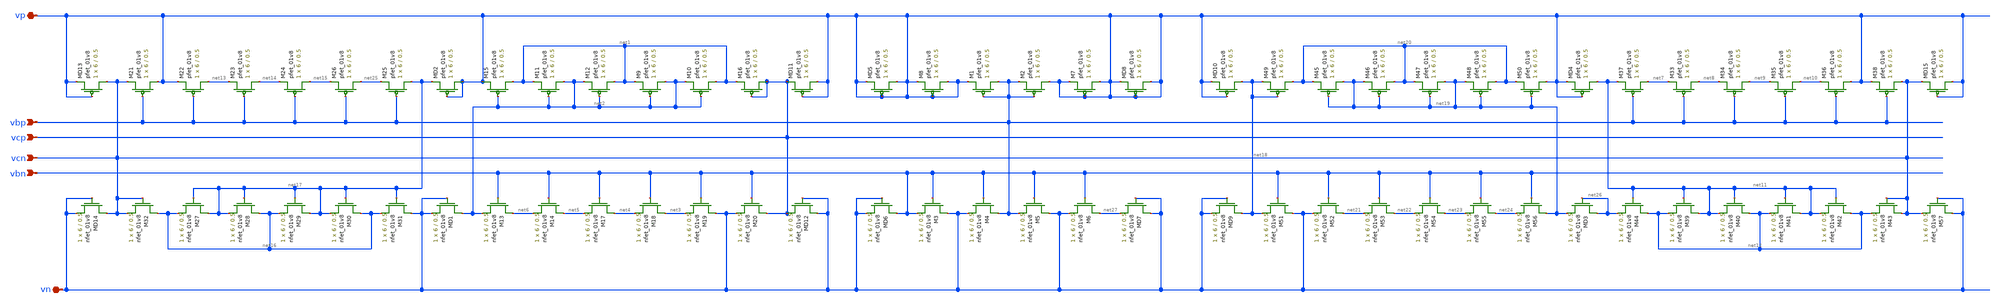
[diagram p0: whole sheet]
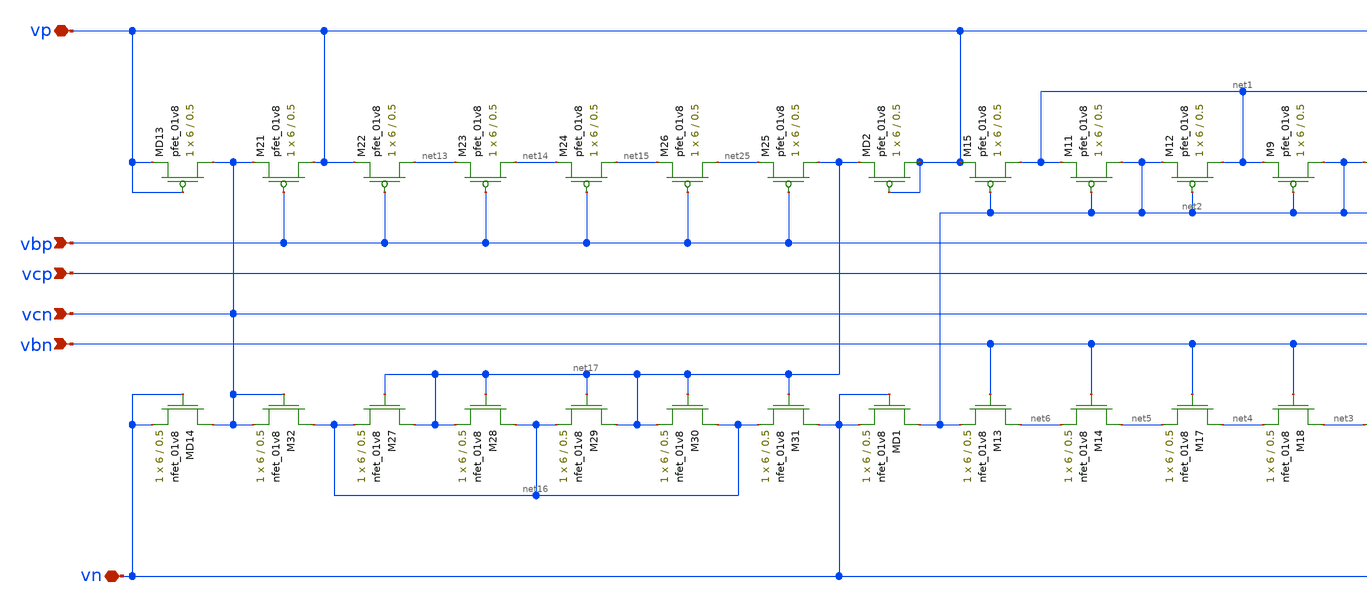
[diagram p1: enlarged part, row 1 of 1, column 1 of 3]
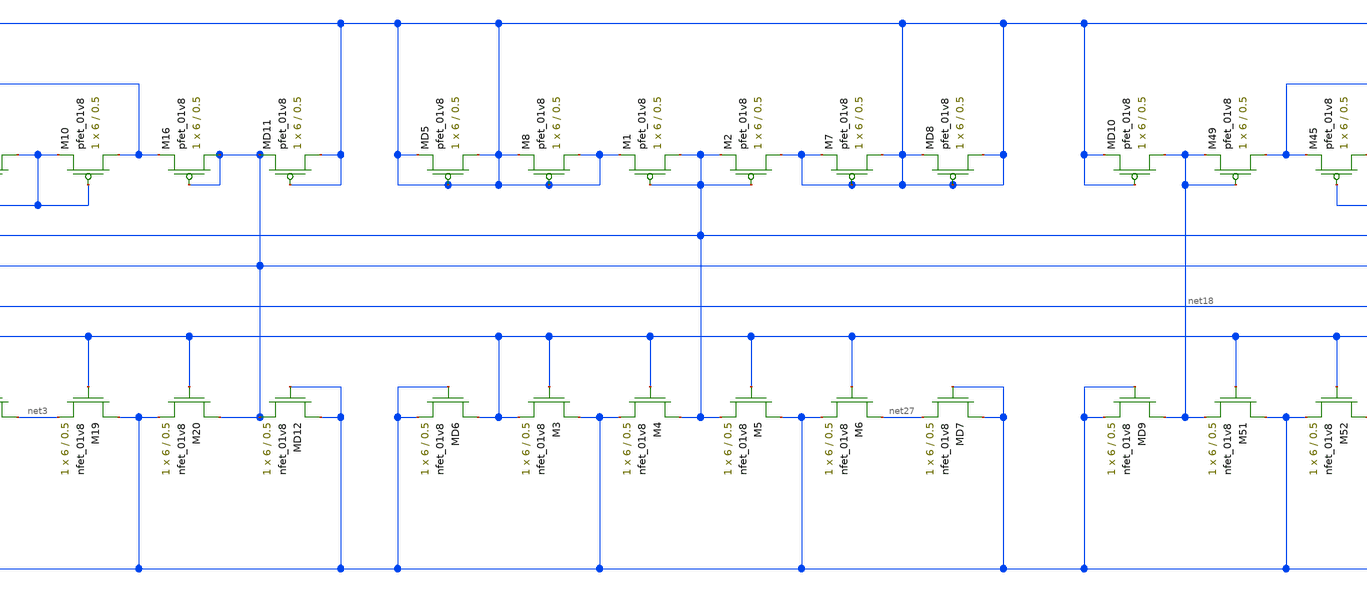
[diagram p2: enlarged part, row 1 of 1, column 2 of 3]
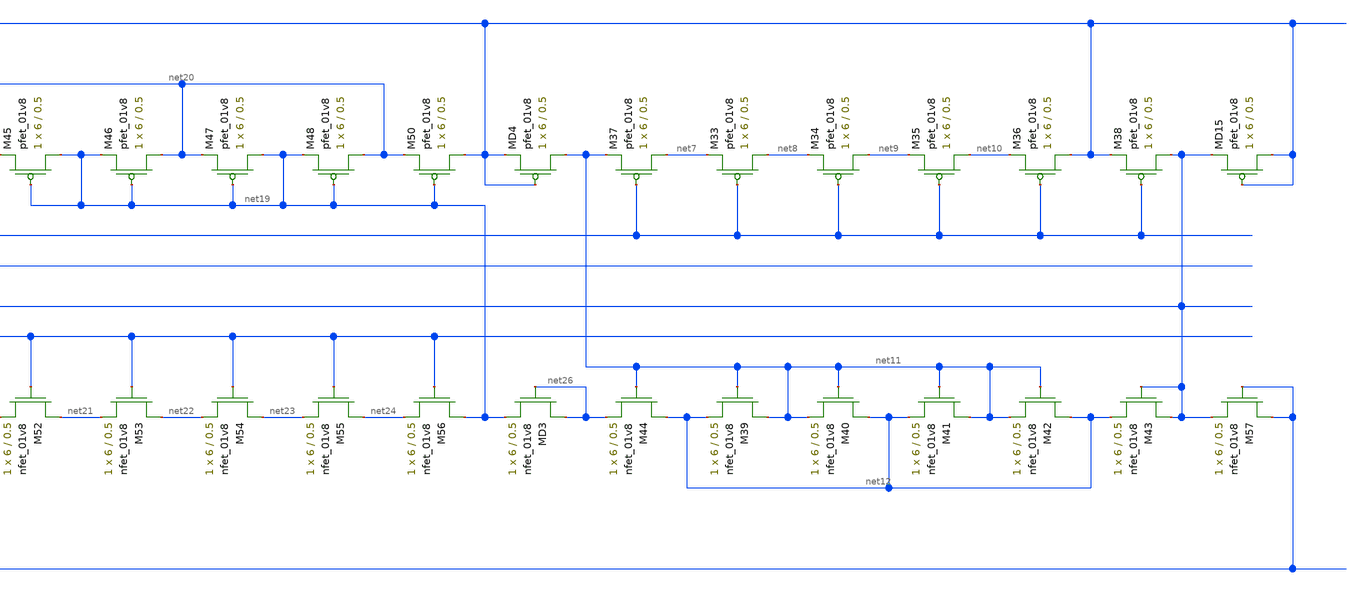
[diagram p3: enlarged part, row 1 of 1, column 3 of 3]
** sch_path: mini_proj_3/schematic/bias_generator.sch
**.subckt bias_generator vp vn vbn vcn vcp vbp
*.iopin vp
*.iopin vn
*.ipin vbn
*.ipin vcn
*.ipin vcp
*.ipin vbp
XM3 vn vbn vbn GND sky130_fd_pr__nfet_01v8 L=0.5 W=6 nf=1 ad='int((nf+1)/2) * W/nf * 0.29' as='int((nf+2)/2) * W/nf * 0.29'
+ pd='2*int((nf+1)/2) * (W/nf + 0.29)' ps='2*int((nf+2)/2) * (W/nf + 0.29)' nrd='0.29 / W' nrs='0.29 / W'
+ sa=0 sb=0 sd=0 mult=1 m=1
XM8 vp vp vp VDD sky130_fd_pr__pfet_01v8 L=0.5 W=6 nf=1 ad='int((nf+1)/2) * W/nf * 0.29' as='int((nf+2)/2) * W/nf * 0.29'
+ pd='2*int((nf+1)/2) * (W/nf + 0.29)' ps='2*int((nf+2)/2) * (W/nf + 0.29)' nrd='0.29 / W' nrs='0.29 / W'
+ sa=0 sb=0 sd=0 mult=1 m=1
XM1 vbp vbp vp VDD sky130_fd_pr__pfet_01v8 L=0.5 W=6 nf=1 ad='int((nf+1)/2) * W/nf * 0.29' as='int((nf+2)/2) * W/nf * 0.29'
+ pd='2*int((nf+1)/2) * (W/nf + 0.29)' ps='2*int((nf+2)/2) * (W/nf + 0.29)' nrd='0.29 / W' nrs='0.29 / W'
+ sa=0 sb=0 sd=0 mult=1 m=1
XM2 vp vbp vbp VDD sky130_fd_pr__pfet_01v8 L=0.5 W=6 nf=1 ad='int((nf+1)/2) * W/nf * 0.29' as='int((nf+2)/2) * W/nf * 0.29'
+ pd='2*int((nf+1)/2) * (W/nf + 0.29)' ps='2*int((nf+2)/2) * (W/nf + 0.29)' nrd='0.29 / W' nrs='0.29 / W'
+ sa=0 sb=0 sd=0 mult=1 m=1
XM7 vp vp vp VDD sky130_fd_pr__pfet_01v8 L=0.5 W=6 nf=1 ad='int((nf+1)/2) * W/nf * 0.29' as='int((nf+2)/2) * W/nf * 0.29'
+ pd='2*int((nf+1)/2) * (W/nf + 0.29)' ps='2*int((nf+2)/2) * (W/nf + 0.29)' nrd='0.29 / W' nrs='0.29 / W'
+ sa=0 sb=0 sd=0 mult=1 m=1
XM4 vbp vbn vn GND sky130_fd_pr__nfet_01v8 L=0.5 W=6 nf=1 ad='int((nf+1)/2) * W/nf * 0.29' as='int((nf+2)/2) * W/nf * 0.29'
+ pd='2*int((nf+1)/2) * (W/nf + 0.29)' ps='2*int((nf+2)/2) * (W/nf + 0.29)' nrd='0.29 / W' nrs='0.29 / W'
+ sa=0 sb=0 sd=0 mult=1 m=1
XM5 vn vbn vbp GND sky130_fd_pr__nfet_01v8 L=0.5 W=6 nf=1 ad='int((nf+1)/2) * W/nf * 0.29' as='int((nf+2)/2) * W/nf * 0.29'
+ pd='2*int((nf+1)/2) * (W/nf + 0.29)' ps='2*int((nf+2)/2) * (W/nf + 0.29)' nrd='0.29 / W' nrs='0.29 / W'
+ sa=0 sb=0 sd=0 mult=1 m=1
XM6 net27 vbn vn GND sky130_fd_pr__nfet_01v8 L=0.5 W=6 nf=1 ad='int((nf+1)/2) * W/nf * 0.29' as='int((nf+2)/2) * W/nf * 0.29'
+ pd='2*int((nf+1)/2) * (W/nf + 0.29)' ps='2*int((nf+2)/2) * (W/nf + 0.29)' nrd='0.29 / W' nrs='0.29 / W'
+ sa=0 sb=0 sd=0 mult=1 m=1
XM11 net2 net2 net1 VDD sky130_fd_pr__pfet_01v8 L=0.5 W=6 nf=1 ad='int((nf+1)/2) * W/nf * 0.29' as='int((nf+2)/2) * W/nf * 0.29'
+ pd='2*int((nf+1)/2) * (W/nf + 0.29)' ps='2*int((nf+2)/2) * (W/nf + 0.29)' nrd='0.29 / W' nrs='0.29 / W'
+ sa=0 sb=0 sd=0 mult=1 m=1
XM12 net1 net2 net2 VDD sky130_fd_pr__pfet_01v8 L=0.5 W=6 nf=1 ad='int((nf+1)/2) * W/nf * 0.29' as='int((nf+2)/2) * W/nf * 0.29'
+ pd='2*int((nf+1)/2) * (W/nf + 0.29)' ps='2*int((nf+2)/2) * (W/nf + 0.29)' nrd='0.29 / W' nrs='0.29 / W'
+ sa=0 sb=0 sd=0 mult=1 m=1
XM9 net2 net2 net1 VDD sky130_fd_pr__pfet_01v8 L=0.5 W=6 nf=1 ad='int((nf+1)/2) * W/nf * 0.29' as='int((nf+2)/2) * W/nf * 0.29'
+ pd='2*int((nf+1)/2) * (W/nf + 0.29)' ps='2*int((nf+2)/2) * (W/nf + 0.29)' nrd='0.29 / W' nrs='0.29 / W'
+ sa=0 sb=0 sd=0 mult=1 m=1
XM10 net1 net2 net2 VDD sky130_fd_pr__pfet_01v8 L=0.5 W=6 nf=1 ad='int((nf+1)/2) * W/nf * 0.29' as='int((nf+2)/2) * W/nf * 0.29'
+ pd='2*int((nf+1)/2) * (W/nf + 0.29)' ps='2*int((nf+2)/2) * (W/nf + 0.29)' nrd='0.29 / W' nrs='0.29 / W'
+ sa=0 sb=0 sd=0 mult=1 m=1
XM15 net1 net2 vp VDD sky130_fd_pr__pfet_01v8 L=0.5 W=6 nf=1 ad='int((nf+1)/2) * W/nf * 0.29' as='int((nf+2)/2) * W/nf * 0.29'
+ pd='2*int((nf+1)/2) * (W/nf + 0.29)' ps='2*int((nf+2)/2) * (W/nf + 0.29)' nrd='0.29 / W' nrs='0.29 / W'
+ sa=0 sb=0 sd=0 mult=1 m=1
XM16 vcp vcp net1 VDD sky130_fd_pr__pfet_01v8 L=0.5 W=6 nf=1 ad='int((nf+1)/2) * W/nf * 0.29' as='int((nf+2)/2) * W/nf * 0.29'
+ pd='2*int((nf+1)/2) * (W/nf + 0.29)' ps='2*int((nf+2)/2) * (W/nf + 0.29)' nrd='0.29 / W' nrs='0.29 / W'
+ sa=0 sb=0 sd=0 mult=1 m=1
XM13 net6 vbn net2 GND sky130_fd_pr__nfet_01v8 L=0.5 W=6 nf=1 ad='int((nf+1)/2) * W/nf * 0.29' as='int((nf+2)/2) * W/nf * 0.29'
+ pd='2*int((nf+1)/2) * (W/nf + 0.29)' ps='2*int((nf+2)/2) * (W/nf + 0.29)' nrd='0.29 / W' nrs='0.29 / W'
+ sa=0 sb=0 sd=0 mult=1 m=1
XM14 net5 vbn net6 GND sky130_fd_pr__nfet_01v8 L=0.5 W=6 nf=1 ad='int((nf+1)/2) * W/nf * 0.29' as='int((nf+2)/2) * W/nf * 0.29'
+ pd='2*int((nf+1)/2) * (W/nf + 0.29)' ps='2*int((nf+2)/2) * (W/nf + 0.29)' nrd='0.29 / W' nrs='0.29 / W'
+ sa=0 sb=0 sd=0 mult=1 m=1
XM17 net4 vbn net5 GND sky130_fd_pr__nfet_01v8 L=0.5 W=6 nf=1 ad='int((nf+1)/2) * W/nf * 0.29' as='int((nf+2)/2) * W/nf * 0.29'
+ pd='2*int((nf+1)/2) * (W/nf + 0.29)' ps='2*int((nf+2)/2) * (W/nf + 0.29)' nrd='0.29 / W' nrs='0.29 / W'
+ sa=0 sb=0 sd=0 mult=1 m=1
XM18 net3 vbn net4 GND sky130_fd_pr__nfet_01v8 L=0.5 W=6 nf=1 ad='int((nf+1)/2) * W/nf * 0.29' as='int((nf+2)/2) * W/nf * 0.29'
+ pd='2*int((nf+1)/2) * (W/nf + 0.29)' ps='2*int((nf+2)/2) * (W/nf + 0.29)' nrd='0.29 / W' nrs='0.29 / W'
+ sa=0 sb=0 sd=0 mult=1 m=1
XM19 vn vbn net3 GND sky130_fd_pr__nfet_01v8 L=0.5 W=6 nf=1 ad='int((nf+1)/2) * W/nf * 0.29' as='int((nf+2)/2) * W/nf * 0.29'
+ pd='2*int((nf+1)/2) * (W/nf + 0.29)' ps='2*int((nf+2)/2) * (W/nf + 0.29)' nrd='0.29 / W' nrs='0.29 / W'
+ sa=0 sb=0 sd=0 mult=1 m=1
XM20 vcp vbn vn GND sky130_fd_pr__nfet_01v8 L=0.5 W=6 nf=1 ad='int((nf+1)/2) * W/nf * 0.29' as='int((nf+2)/2) * W/nf * 0.29'
+ pd='2*int((nf+1)/2) * (W/nf + 0.29)' ps='2*int((nf+2)/2) * (W/nf + 0.29)' nrd='0.29 / W' nrs='0.29 / W'
+ sa=0 sb=0 sd=0 mult=1 m=1
XM33 net8 vbp net7 VDD sky130_fd_pr__pfet_01v8 L=0.5 W=6 nf=1 ad='int((nf+1)/2) * W/nf * 0.29' as='int((nf+2)/2) * W/nf * 0.29'
+ pd='2*int((nf+1)/2) * (W/nf + 0.29)' ps='2*int((nf+2)/2) * (W/nf + 0.29)' nrd='0.29 / W' nrs='0.29 / W'
+ sa=0 sb=0 sd=0 mult=1 m=1
XM34 net9 vbp net8 VDD sky130_fd_pr__pfet_01v8 L=0.5 W=6 nf=1 ad='int((nf+1)/2) * W/nf * 0.29' as='int((nf+2)/2) * W/nf * 0.29'
+ pd='2*int((nf+1)/2) * (W/nf + 0.29)' ps='2*int((nf+2)/2) * (W/nf + 0.29)' nrd='0.29 / W' nrs='0.29 / W'
+ sa=0 sb=0 sd=0 mult=1 m=1
XM35 net10 vbp net9 VDD sky130_fd_pr__pfet_01v8 L=0.5 W=6 nf=1 ad='int((nf+1)/2) * W/nf * 0.29' as='int((nf+2)/2) * W/nf * 0.29'
+ pd='2*int((nf+1)/2) * (W/nf + 0.29)' ps='2*int((nf+2)/2) * (W/nf + 0.29)' nrd='0.29 / W' nrs='0.29 / W'
+ sa=0 sb=0 sd=0 mult=1 m=1
XM36 vp vbp net10 VDD sky130_fd_pr__pfet_01v8 L=0.5 W=6 nf=1 ad='int((nf+1)/2) * W/nf * 0.29' as='int((nf+2)/2) * W/nf * 0.29'
+ pd='2*int((nf+1)/2) * (W/nf + 0.29)' ps='2*int((nf+2)/2) * (W/nf + 0.29)' nrd='0.29 / W' nrs='0.29 / W'
+ sa=0 sb=0 sd=0 mult=1 m=1
XM37 net7 vbp net11 VDD sky130_fd_pr__pfet_01v8 L=0.5 W=6 nf=1 ad='int((nf+1)/2) * W/nf * 0.29' as='int((nf+2)/2) * W/nf * 0.29'
+ pd='2*int((nf+1)/2) * (W/nf + 0.29)' ps='2*int((nf+2)/2) * (W/nf + 0.29)' nrd='0.29 / W' nrs='0.29 / W'
+ sa=0 sb=0 sd=0 mult=1 m=1
XM38 vcn vbp vp VDD sky130_fd_pr__pfet_01v8 L=0.5 W=6 nf=1 ad='int((nf+1)/2) * W/nf * 0.29' as='int((nf+2)/2) * W/nf * 0.29'
+ pd='2*int((nf+1)/2) * (W/nf + 0.29)' ps='2*int((nf+2)/2) * (W/nf + 0.29)' nrd='0.29 / W' nrs='0.29 / W'
+ sa=0 sb=0 sd=0 mult=1 m=1
XM39 net11 net11 net12 GND sky130_fd_pr__nfet_01v8 L=0.5 W=6 nf=1 ad='int((nf+1)/2) * W/nf * 0.29' as='int((nf+2)/2) * W/nf * 0.29'
+ pd='2*int((nf+1)/2) * (W/nf + 0.29)' ps='2*int((nf+2)/2) * (W/nf + 0.29)' nrd='0.29 / W' nrs='0.29 / W'
+ sa=0 sb=0 sd=0 mult=1 m=1
XM40 net12 net11 net11 GND sky130_fd_pr__nfet_01v8 L=0.5 W=6 nf=1 ad='int((nf+1)/2) * W/nf * 0.29' as='int((nf+2)/2) * W/nf * 0.29'
+ pd='2*int((nf+1)/2) * (W/nf + 0.29)' ps='2*int((nf+2)/2) * (W/nf + 0.29)' nrd='0.29 / W' nrs='0.29 / W'
+ sa=0 sb=0 sd=0 mult=1 m=1
XM41 net11 net11 net12 GND sky130_fd_pr__nfet_01v8 L=0.5 W=6 nf=1 ad='int((nf+1)/2) * W/nf * 0.29' as='int((nf+2)/2) * W/nf * 0.29'
+ pd='2*int((nf+1)/2) * (W/nf + 0.29)' ps='2*int((nf+2)/2) * (W/nf + 0.29)' nrd='0.29 / W' nrs='0.29 / W'
+ sa=0 sb=0 sd=0 mult=1 m=1
XM42 net12 net11 net11 GND sky130_fd_pr__nfet_01v8 L=0.5 W=6 nf=1 ad='int((nf+1)/2) * W/nf * 0.29' as='int((nf+2)/2) * W/nf * 0.29'
+ pd='2*int((nf+1)/2) * (W/nf + 0.29)' ps='2*int((nf+2)/2) * (W/nf + 0.29)' nrd='0.29 / W' nrs='0.29 / W'
+ sa=0 sb=0 sd=0 mult=1 m=1
XM43 vcn vcn net12 GND sky130_fd_pr__nfet_01v8 L=0.5 W=6 nf=1 ad='int((nf+1)/2) * W/nf * 0.29' as='int((nf+2)/2) * W/nf * 0.29'
+ pd='2*int((nf+1)/2) * (W/nf + 0.29)' ps='2*int((nf+2)/2) * (W/nf + 0.29)' nrd='0.29 / W' nrs='0.29 / W'
+ sa=0 sb=0 sd=0 mult=1 m=1
XM44 net12 net11 net26 GND sky130_fd_pr__nfet_01v8 L=0.5 W=6 nf=1 ad='int((nf+1)/2) * W/nf * 0.29' as='int((nf+2)/2) * W/nf * 0.29'
+ pd='2*int((nf+1)/2) * (W/nf + 0.29)' ps='2*int((nf+2)/2) * (W/nf + 0.29)' nrd='0.29 / W' nrs='0.29 / W'
+ sa=0 sb=0 sd=0 mult=1 m=1
XM21 vp vbp vcn VDD sky130_fd_pr__pfet_01v8 L=0.5 W=6 nf=1 ad='int((nf+1)/2) * W/nf * 0.29' as='int((nf+2)/2) * W/nf * 0.29'
+ pd='2*int((nf+1)/2) * (W/nf + 0.29)' ps='2*int((nf+2)/2) * (W/nf + 0.29)' nrd='0.29 / W' nrs='0.29 / W'
+ sa=0 sb=0 sd=0 mult=1 m=1
XM22 net13 vbp vp VDD sky130_fd_pr__pfet_01v8 L=0.5 W=6 nf=1 ad='int((nf+1)/2) * W/nf * 0.29' as='int((nf+2)/2) * W/nf * 0.29'
+ pd='2*int((nf+1)/2) * (W/nf + 0.29)' ps='2*int((nf+2)/2) * (W/nf + 0.29)' nrd='0.29 / W' nrs='0.29 / W'
+ sa=0 sb=0 sd=0 mult=1 m=1
XM23 net14 vbp net13 VDD sky130_fd_pr__pfet_01v8 L=0.5 W=6 nf=1 ad='int((nf+1)/2) * W/nf * 0.29' as='int((nf+2)/2) * W/nf * 0.29'
+ pd='2*int((nf+1)/2) * (W/nf + 0.29)' ps='2*int((nf+2)/2) * (W/nf + 0.29)' nrd='0.29 / W' nrs='0.29 / W'
+ sa=0 sb=0 sd=0 mult=1 m=1
XM24 net15 vbp net14 VDD sky130_fd_pr__pfet_01v8 L=0.5 W=6 nf=1 ad='int((nf+1)/2) * W/nf * 0.29' as='int((nf+2)/2) * W/nf * 0.29'
+ pd='2*int((nf+1)/2) * (W/nf + 0.29)' ps='2*int((nf+2)/2) * (W/nf + 0.29)' nrd='0.29 / W' nrs='0.29 / W'
+ sa=0 sb=0 sd=0 mult=1 m=1
XM25 net17 vbp net25 VDD sky130_fd_pr__pfet_01v8 L=0.5 W=6 nf=1 ad='int((nf+1)/2) * W/nf * 0.29' as='int((nf+2)/2) * W/nf * 0.29'
+ pd='2*int((nf+1)/2) * (W/nf + 0.29)' ps='2*int((nf+2)/2) * (W/nf + 0.29)' nrd='0.29 / W' nrs='0.29 / W'
+ sa=0 sb=0 sd=0 mult=1 m=1
XM26 net25 vbp net15 VDD sky130_fd_pr__pfet_01v8 L=0.5 W=6 nf=1 ad='int((nf+1)/2) * W/nf * 0.29' as='int((nf+2)/2) * W/nf * 0.29'
+ pd='2*int((nf+1)/2) * (W/nf + 0.29)' ps='2*int((nf+2)/2) * (W/nf + 0.29)' nrd='0.29 / W' nrs='0.29 / W'
+ sa=0 sb=0 sd=0 mult=1 m=1
XM27 net17 net17 net16 GND sky130_fd_pr__nfet_01v8 L=0.5 W=6 nf=1 ad='int((nf+1)/2) * W/nf * 0.29' as='int((nf+2)/2) * W/nf * 0.29'
+ pd='2*int((nf+1)/2) * (W/nf + 0.29)' ps='2*int((nf+2)/2) * (W/nf + 0.29)' nrd='0.29 / W' nrs='0.29 / W'
+ sa=0 sb=0 sd=0 mult=1 m=1
XM28 net16 net17 net17 GND sky130_fd_pr__nfet_01v8 L=0.5 W=6 nf=1 ad='int((nf+1)/2) * W/nf * 0.29' as='int((nf+2)/2) * W/nf * 0.29'
+ pd='2*int((nf+1)/2) * (W/nf + 0.29)' ps='2*int((nf+2)/2) * (W/nf + 0.29)' nrd='0.29 / W' nrs='0.29 / W'
+ sa=0 sb=0 sd=0 mult=1 m=1
XM29 net17 net17 net16 GND sky130_fd_pr__nfet_01v8 L=0.5 W=6 nf=1 ad='int((nf+1)/2) * W/nf * 0.29' as='int((nf+2)/2) * W/nf * 0.29'
+ pd='2*int((nf+1)/2) * (W/nf + 0.29)' ps='2*int((nf+2)/2) * (W/nf + 0.29)' nrd='0.29 / W' nrs='0.29 / W'
+ sa=0 sb=0 sd=0 mult=1 m=1
XM30 net16 net17 net17 GND sky130_fd_pr__nfet_01v8 L=0.5 W=6 nf=1 ad='int((nf+1)/2) * W/nf * 0.29' as='int((nf+2)/2) * W/nf * 0.29'
+ pd='2*int((nf+1)/2) * (W/nf + 0.29)' ps='2*int((nf+2)/2) * (W/nf + 0.29)' nrd='0.29 / W' nrs='0.29 / W'
+ sa=0 sb=0 sd=0 mult=1 m=1
XM31 vn net17 net16 GND sky130_fd_pr__nfet_01v8 L=0.5 W=6 nf=1 ad='int((nf+1)/2) * W/nf * 0.29' as='int((nf+2)/2) * W/nf * 0.29'
+ pd='2*int((nf+1)/2) * (W/nf + 0.29)' ps='2*int((nf+2)/2) * (W/nf + 0.29)' nrd='0.29 / W' nrs='0.29 / W'
+ sa=0 sb=0 sd=0 mult=1 m=1
XM32 net16 vcn vcn GND sky130_fd_pr__nfet_01v8 L=0.5 W=6 nf=1 ad='int((nf+1)/2) * W/nf * 0.29' as='int((nf+2)/2) * W/nf * 0.29'
+ pd='2*int((nf+1)/2) * (W/nf + 0.29)' ps='2*int((nf+2)/2) * (W/nf + 0.29)' nrd='0.29 / W' nrs='0.29 / W'
+ sa=0 sb=0 sd=0 mult=1 m=1
XM45 net19 net19 net20 VDD sky130_fd_pr__pfet_01v8 L=0.5 W=6 nf=1 ad='int((nf+1)/2) * W/nf * 0.29' as='int((nf+2)/2) * W/nf * 0.29'
+ pd='2*int((nf+1)/2) * (W/nf + 0.29)' ps='2*int((nf+2)/2) * (W/nf + 0.29)' nrd='0.29 / W' nrs='0.29 / W'
+ sa=0 sb=0 sd=0 mult=1 m=1
XM46 net20 net19 net19 VDD sky130_fd_pr__pfet_01v8 L=0.5 W=6 nf=1 ad='int((nf+1)/2) * W/nf * 0.29' as='int((nf+2)/2) * W/nf * 0.29'
+ pd='2*int((nf+1)/2) * (W/nf + 0.29)' ps='2*int((nf+2)/2) * (W/nf + 0.29)' nrd='0.29 / W' nrs='0.29 / W'
+ sa=0 sb=0 sd=0 mult=1 m=1
XM47 net19 net19 net20 VDD sky130_fd_pr__pfet_01v8 L=0.5 W=6 nf=1 ad='int((nf+1)/2) * W/nf * 0.29' as='int((nf+2)/2) * W/nf * 0.29'
+ pd='2*int((nf+1)/2) * (W/nf + 0.29)' ps='2*int((nf+2)/2) * (W/nf + 0.29)' nrd='0.29 / W' nrs='0.29 / W'
+ sa=0 sb=0 sd=0 mult=1 m=1
XM48 net20 net19 net19 VDD sky130_fd_pr__pfet_01v8 L=0.5 W=6 nf=1 ad='int((nf+1)/2) * W/nf * 0.29' as='int((nf+2)/2) * W/nf * 0.29'
+ pd='2*int((nf+1)/2) * (W/nf + 0.29)' ps='2*int((nf+2)/2) * (W/nf + 0.29)' nrd='0.29 / W' nrs='0.29 / W'
+ sa=0 sb=0 sd=0 mult=1 m=1
XM49 net20 net18 net18 VDD sky130_fd_pr__pfet_01v8 L=0.5 W=6 nf=1 ad='int((nf+1)/2) * W/nf * 0.29' as='int((nf+2)/2) * W/nf * 0.29'
+ pd='2*int((nf+1)/2) * (W/nf + 0.29)' ps='2*int((nf+2)/2) * (W/nf + 0.29)' nrd='0.29 / W' nrs='0.29 / W'
+ sa=0 sb=0 sd=0 mult=1 m=1
XM50 vp net19 net20 VDD sky130_fd_pr__pfet_01v8 L=0.5 W=6 nf=1 ad='int((nf+1)/2) * W/nf * 0.29' as='int((nf+2)/2) * W/nf * 0.29'
+ pd='2*int((nf+1)/2) * (W/nf + 0.29)' ps='2*int((nf+2)/2) * (W/nf + 0.29)' nrd='0.29 / W' nrs='0.29 / W'
+ sa=0 sb=0 sd=0 mult=1 m=1
XM51 vn vbn net18 GND sky130_fd_pr__nfet_01v8 L=0.5 W=6 nf=1 ad='int((nf+1)/2) * W/nf * 0.29' as='int((nf+2)/2) * W/nf * 0.29'
+ pd='2*int((nf+1)/2) * (W/nf + 0.29)' ps='2*int((nf+2)/2) * (W/nf + 0.29)' nrd='0.29 / W' nrs='0.29 / W'
+ sa=0 sb=0 sd=0 mult=1 m=1
XM52 net21 vbn vn GND sky130_fd_pr__nfet_01v8 L=0.5 W=6 nf=1 ad='int((nf+1)/2) * W/nf * 0.29' as='int((nf+2)/2) * W/nf * 0.29'
+ pd='2*int((nf+1)/2) * (W/nf + 0.29)' ps='2*int((nf+2)/2) * (W/nf + 0.29)' nrd='0.29 / W' nrs='0.29 / W'
+ sa=0 sb=0 sd=0 mult=1 m=1
XM53 net22 vbn net21 GND sky130_fd_pr__nfet_01v8 L=0.5 W=6 nf=1 ad='int((nf+1)/2) * W/nf * 0.29' as='int((nf+2)/2) * W/nf * 0.29'
+ pd='2*int((nf+1)/2) * (W/nf + 0.29)' ps='2*int((nf+2)/2) * (W/nf + 0.29)' nrd='0.29 / W' nrs='0.29 / W'
+ sa=0 sb=0 sd=0 mult=1 m=1
XM54 net23 vbn net22 GND sky130_fd_pr__nfet_01v8 L=0.5 W=6 nf=1 ad='int((nf+1)/2) * W/nf * 0.29' as='int((nf+2)/2) * W/nf * 0.29'
+ pd='2*int((nf+1)/2) * (W/nf + 0.29)' ps='2*int((nf+2)/2) * (W/nf + 0.29)' nrd='0.29 / W' nrs='0.29 / W'
+ sa=0 sb=0 sd=0 mult=1 m=1
XM55 net24 vbn net23 GND sky130_fd_pr__nfet_01v8 L=0.5 W=6 nf=1 ad='int((nf+1)/2) * W/nf * 0.29' as='int((nf+2)/2) * W/nf * 0.29'
+ pd='2*int((nf+1)/2) * (W/nf + 0.29)' ps='2*int((nf+2)/2) * (W/nf + 0.29)' nrd='0.29 / W' nrs='0.29 / W'
+ sa=0 sb=0 sd=0 mult=1 m=1
XM56 net19 vbn net24 GND sky130_fd_pr__nfet_01v8 L=0.5 W=6 nf=1 ad='int((nf+1)/2) * W/nf * 0.29' as='int((nf+2)/2) * W/nf * 0.29'
+ pd='2*int((nf+1)/2) * (W/nf + 0.29)' ps='2*int((nf+2)/2) * (W/nf + 0.29)' nrd='0.29 / W' nrs='0.29 / W'
+ sa=0 sb=0 sd=0 mult=1 m=1
XMD1 net2 vn vn GND sky130_fd_pr__nfet_01v8 L=0.5 W=6 nf=1 ad='int((nf+1)/2) * W/nf * 0.29' as='int((nf+2)/2) * W/nf * 0.29'
+ pd='2*int((nf+1)/2) * (W/nf + 0.29)' ps='2*int((nf+2)/2) * (W/nf + 0.29)' nrd='0.29 / W' nrs='0.29 / W'
+ sa=0 sb=0 sd=0 mult=1 m=1
XMD2 vp vp net17 VDD sky130_fd_pr__pfet_01v8 L=0.5 W=6 nf=1 ad='int((nf+1)/2) * W/nf * 0.29' as='int((nf+2)/2) * W/nf * 0.29'
+ pd='2*int((nf+1)/2) * (W/nf + 0.29)' ps='2*int((nf+2)/2) * (W/nf + 0.29)' nrd='0.29 / W' nrs='0.29 / W'
+ sa=0 sb=0 sd=0 mult=1 m=1
XMD3 net26 net26 net19 GND sky130_fd_pr__nfet_01v8 L=0.5 W=6 nf=1 ad='int((nf+1)/2) * W/nf * 0.29' as='int((nf+2)/2) * W/nf * 0.29'
+ pd='2*int((nf+1)/2) * (W/nf + 0.29)' ps='2*int((nf+2)/2) * (W/nf + 0.29)' nrd='0.29 / W' nrs='0.29 / W'
+ sa=0 sb=0 sd=0 mult=1 m=1
XMD4 net11 vp vp VDD sky130_fd_pr__pfet_01v8 L=0.5 W=6 nf=1 ad='int((nf+1)/2) * W/nf * 0.29' as='int((nf+2)/2) * W/nf * 0.29'
+ pd='2*int((nf+1)/2) * (W/nf + 0.29)' ps='2*int((nf+2)/2) * (W/nf + 0.29)' nrd='0.29 / W' nrs='0.29 / W'
+ sa=0 sb=0 sd=0 mult=1 m=1
XMD7 vn vn net27 GND sky130_fd_pr__nfet_01v8 L=0.5 W=6 nf=1 ad='int((nf+1)/2) * W/nf * 0.29' as='int((nf+2)/2) * W/nf * 0.29'
+ pd='2*int((nf+1)/2) * (W/nf + 0.29)' ps='2*int((nf+2)/2) * (W/nf + 0.29)' nrd='0.29 / W' nrs='0.29 / W'
+ sa=0 sb=0 sd=0 mult=1 m=1
XMD8 vp vp vp VDD sky130_fd_pr__pfet_01v8 L=0.5 W=6 nf=1 ad='int((nf+1)/2) * W/nf * 0.29' as='int((nf+2)/2) * W/nf * 0.29'
+ pd='2*int((nf+1)/2) * (W/nf + 0.29)' ps='2*int((nf+2)/2) * (W/nf + 0.29)' nrd='0.29 / W' nrs='0.29 / W'
+ sa=0 sb=0 sd=0 mult=1 m=1
XMD9 net18 vn vn GND sky130_fd_pr__nfet_01v8 L=0.5 W=6 nf=1 ad='int((nf+1)/2) * W/nf * 0.29' as='int((nf+2)/2) * W/nf * 0.29'
+ pd='2*int((nf+1)/2) * (W/nf + 0.29)' ps='2*int((nf+2)/2) * (W/nf + 0.29)' nrd='0.29 / W' nrs='0.29 / W'
+ sa=0 sb=0 sd=0 mult=1 m=1
XMD10 net18 vp vp VDD sky130_fd_pr__pfet_01v8 L=0.5 W=6 nf=1 ad='int((nf+1)/2) * W/nf * 0.29' as='int((nf+2)/2) * W/nf * 0.29'
+ pd='2*int((nf+1)/2) * (W/nf + 0.29)' ps='2*int((nf+2)/2) * (W/nf + 0.29)' nrd='0.29 / W' nrs='0.29 / W'
+ sa=0 sb=0 sd=0 mult=1 m=1
XMD5 vp vp vp VDD sky130_fd_pr__pfet_01v8 L=0.5 W=6 nf=1 ad='int((nf+1)/2) * W/nf * 0.29' as='int((nf+2)/2) * W/nf * 0.29'
+ pd='2*int((nf+1)/2) * (W/nf + 0.29)' ps='2*int((nf+2)/2) * (W/nf + 0.29)' nrd='0.29 / W' nrs='0.29 / W'
+ sa=0 sb=0 sd=0 mult=1 m=1
XMD6 vbn vn vn GND sky130_fd_pr__nfet_01v8 L=0.5 W=6 nf=1 ad='int((nf+1)/2) * W/nf * 0.29' as='int((nf+2)/2) * W/nf * 0.29'
+ pd='2*int((nf+1)/2) * (W/nf + 0.29)' ps='2*int((nf+2)/2) * (W/nf + 0.29)' nrd='0.29 / W' nrs='0.29 / W'
+ sa=0 sb=0 sd=0 mult=1 m=1
XMD11 vp vp vcp VDD sky130_fd_pr__pfet_01v8 L=0.5 W=6 nf=1 ad='int((nf+1)/2) * W/nf * 0.29' as='int((nf+2)/2) * W/nf * 0.29'
+ pd='2*int((nf+1)/2) * (W/nf + 0.29)' ps='2*int((nf+2)/2) * (W/nf + 0.29)' nrd='0.29 / W' nrs='0.29 / W'
+ sa=0 sb=0 sd=0 mult=1 m=1
XMD12 vn vn vcp GND sky130_fd_pr__nfet_01v8 L=0.5 W=6 nf=1 ad='int((nf+1)/2) * W/nf * 0.29' as='int((nf+2)/2) * W/nf * 0.29'
+ pd='2*int((nf+1)/2) * (W/nf + 0.29)' ps='2*int((nf+2)/2) * (W/nf + 0.29)' nrd='0.29 / W' nrs='0.29 / W'
+ sa=0 sb=0 sd=0 mult=1 m=1
XMD13 vcn vp vp VDD sky130_fd_pr__pfet_01v8 L=0.5 W=6 nf=1 ad='int((nf+1)/2) * W/nf * 0.29' as='int((nf+2)/2) * W/nf * 0.29'
+ pd='2*int((nf+1)/2) * (W/nf + 0.29)' ps='2*int((nf+2)/2) * (W/nf + 0.29)' nrd='0.29 / W' nrs='0.29 / W'
+ sa=0 sb=0 sd=0 mult=1 m=1
XMD14 vcn vn vn GND sky130_fd_pr__nfet_01v8 L=0.5 W=6 nf=1 ad='int((nf+1)/2) * W/nf * 0.29' as='int((nf+2)/2) * W/nf * 0.29'
+ pd='2*int((nf+1)/2) * (W/nf + 0.29)' ps='2*int((nf+2)/2) * (W/nf + 0.29)' nrd='0.29 / W' nrs='0.29 / W'
+ sa=0 sb=0 sd=0 mult=1 m=1
XMD15 vp vp vcn VDD sky130_fd_pr__pfet_01v8 L=0.5 W=6 nf=1 ad='int((nf+1)/2) * W/nf * 0.29' as='int((nf+2)/2) * W/nf * 0.29'
+ pd='2*int((nf+1)/2) * (W/nf + 0.29)' ps='2*int((nf+2)/2) * (W/nf + 0.29)' nrd='0.29 / W' nrs='0.29 / W'
+ sa=0 sb=0 sd=0 mult=1 m=1
XM57 vn vn vcn GND sky130_fd_pr__nfet_01v8 L=0.5 W=6 nf=1 ad='int((nf+1)/2) * W/nf * 0.29' as='int((nf+2)/2) * W/nf * 0.29'
+ pd='2*int((nf+1)/2) * (W/nf + 0.29)' ps='2*int((nf+2)/2) * (W/nf + 0.29)' nrd='0.29 / W' nrs='0.29 / W'
+ sa=0 sb=0 sd=0 mult=1 m=1
**.ends
.end
